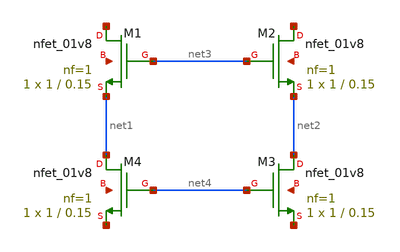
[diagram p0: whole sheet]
** sch_path: xschem/cascade.sch
**.subckt cascade
XM2 net5 net3 net2 net6 sky130_fd_pr__nfet_01v8 L=0.15 W=1 nf=1 ad='int((1 + 1)/2) * 1 / 1 * 0.29' as='int((1 + 2)/2) * 1 / 1 * 0.29'
+ pd='2*int((1 + 1)/2) * (1 / 1 + 0.29)' ps='2*int((1 + 2)/2) * (1 / 1 + 0.29)' nrd='0.29 / 1 ' nrs='0.29 / 1 '
+ sa=0 sb=0 sd=0 mult=1 m=1
XM1 net7 net3 net1 net8 sky130_fd_pr__nfet_01v8 L=0.15 W=1 nf=1 ad='int((1 + 1)/2) * 1 / 1 * 0.29' as='int((1 + 2)/2) * 1 / 1 * 0.29'
+ pd='2*int((1 + 1)/2) * (1 / 1 + 0.29)' ps='2*int((1 + 2)/2) * (1 / 1 + 0.29)' nrd='0.29 / 1 ' nrs='0.29 / 1 '
+ sa=0 sb=0 sd=0 mult=1 m=1
XM3 net2 net4 net9 net10 sky130_fd_pr__nfet_01v8 L=0.15 W=1 nf=1 ad='int((1 + 1)/2) * 1 / 1 * 0.29' as='int((1 + 2)/2) * 1 / 1 * 0.29'
+ pd='2*int((1 + 1)/2) * (1 / 1 + 0.29)' ps='2*int((1 + 2)/2) * (1 / 1 + 0.29)' nrd='0.29 / 1 ' nrs='0.29 / 1 '
+ sa=0 sb=0 sd=0 mult=1 m=1
XM4 net1 net4 net11 net12 sky130_fd_pr__nfet_01v8 L=0.15 W=1 nf=1 ad='int((1 + 1)/2) * 1 / 1 * 0.29'
+ as='int((1 + 2)/2) * 1 / 1 * 0.29' pd='2*int((1 + 1)/2) * (1 / 1 + 0.29)' ps='2*int((1 + 2)/2) * (1 / 1 + 0.29)'
+ nrd='0.29 / 1 ' nrs='0.29 / 1 ' sa=0 sb=0 sd=0 mult=1 m=1
**.ends
.end
